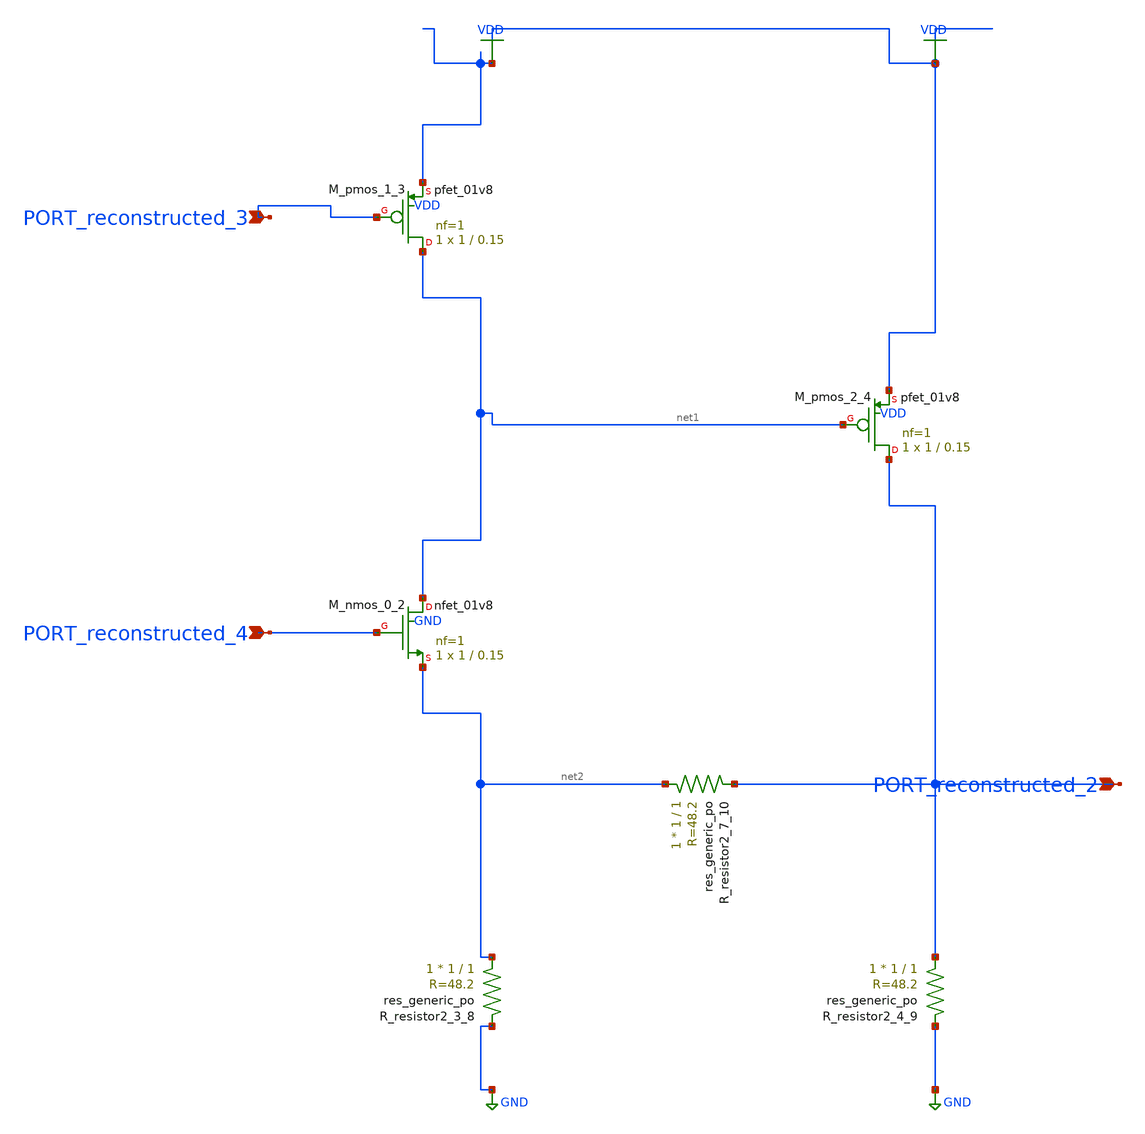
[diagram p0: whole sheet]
** sch_path: schematics/AMSNet/615.sch
**.subckt 615 PORT_reconstructed_2 PORT_reconstructed_3 PORT_reconstructed_4
*.ipin PORT_reconstructed_2
*.ipin PORT_reconstructed_3
*.ipin PORT_reconstructed_4
XM_nmos_0_2 net1 PORT_reconstructed_4 net2 GND sky130_fd_pr__nfet_01v8 L=0.15 W=1 nf=1 ad='int((1 + 1)/2) * 1 / 1 * 0.29'
+ as='int((1 + 2)/2) * 1 / 1 * 0.29' pd='2*int((1 + 1)/2) * (1 / 1 + 0.29)' ps='2*int((1 + 2)/2) * (1 / 1 + 0.29)'
+ nrd='0.29 / 1 ' nrs='0.29 / 1 ' sa=0 sb=0 sd=0 mult=1 m=1
XM_pmos_1_3 net1 PORT_reconstructed_3 VDD VDD sky130_fd_pr__pfet_01v8 L=0.15 W=1 nf=1 ad='int((1 + 1)/2) * 1 / 1 * 0.29'
+ as='int((1 + 2)/2) * 1 / 1 * 0.29' pd='2*int((1 + 1)/2) * (1 / 1 + 0.29)' ps='2*int((1 + 2)/2) * (1 / 1 + 0.29)'
+ nrd='0.29 / 1 ' nrs='0.29 / 1 ' sa=0 sb=0 sd=0 mult=1 m=1
XM_pmos_2_4 PORT_reconstructed_2 net1 VDD VDD sky130_fd_pr__pfet_01v8 L=0.15 W=1 nf=1 ad='int((1 + 1)/2) * 1 / 1 * 0.29'
+ as='int((1 + 2)/2) * 1 / 1 * 0.29' pd='2*int((1 + 1)/2) * (1 / 1 + 0.29)' ps='2*int((1 + 2)/2) * (1 / 1 + 0.29)'
+ nrd='0.29 / 1 ' nrs='0.29 / 1 ' sa=0 sb=0 sd=0 mult=1 m=1
XR_resistor2_3_8 net2 GND sky130_fd_pr__res_generic_po W=1 L=1 m=1
XR_resistor2_4_9 PORT_reconstructed_2 GND sky130_fd_pr__res_generic_po W=1 L=1 m=1
XR_resistor2_7_10 net2 PORT_reconstructed_2 sky130_fd_pr__res_generic_po W=1 L=1 m=1
**.ends
.GLOBAL GND
.GLOBAL VDD
.end
